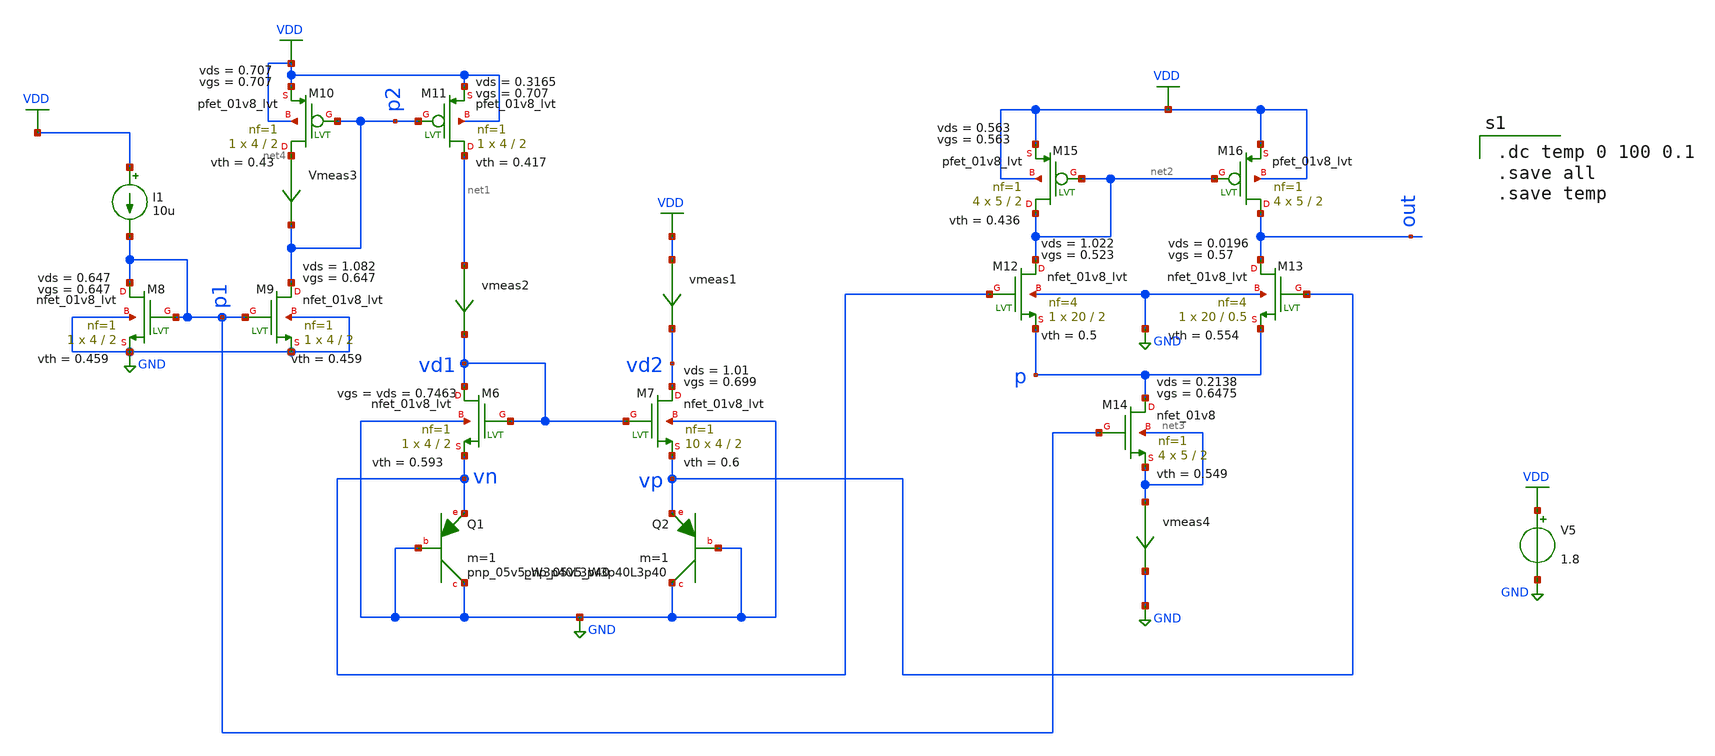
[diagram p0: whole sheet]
** sch_path: ANOTHER_SOLUTIONS_CONSIDERED/ANOTHER_BIAS_FOR_TEMPERATURE_SENSOR/TEMPERATURE_SENSOR/XSCHEM/Temp_Sensor_unbalanced_tb.sch
**.subckt Temp_Sensor_unbalanced_tb
XM6 vd1 vd1 vn GND sky130_fd_pr__nfet_01v8_lvt L=2 W=4 nf=1 ad='int((nf+1)/2) * W/nf * 0.29' as='int((nf+2)/2) * W/nf * 0.29'
+ pd='2*int((nf+1)/2) * (W/nf + 0.29)' ps='2*int((nf+2)/2) * (W/nf + 0.29)' nrd='0.29 / W' nrs='0.29 / W'
+ sa=0 sb=0 sd=0 mult=1 m=1
XQ1 GND GND vn sky130_fd_pr__pnp_05v5_W3p40L3p40 m=1
XM7 vd2 vd1 vp GND sky130_fd_pr__nfet_01v8_lvt L=2 W=4 nf=1 ad='int((nf+1)/2) * W/nf * 0.29' as='int((nf+2)/2) * W/nf * 0.29'
+ pd='2*int((nf+1)/2) * (W/nf + 0.29)' ps='2*int((nf+2)/2) * (W/nf + 0.29)' nrd='0.29 / W' nrs='0.29 / W'
+ sa=0 sb=0 sd=0 mult=10 m=10
XQ2 GND GND vp sky130_fd_pr__pnp_05v5_W3p40L3p40 m=1
V5 VDD GND 1.8
vmeas1 VDD vd2 0
.save i(vmeas1)
vmeas2 net1 vd1 0
.save i(vmeas2)
I1 VDD p1 10u
XM8 p1 p1 GND GND sky130_fd_pr__nfet_01v8_lvt L=2 W=4 nf=1 ad='int((nf+1)/2) * W/nf * 0.29' as='int((nf+2)/2) * W/nf * 0.29'
+ pd='2*int((nf+1)/2) * (W/nf + 0.29)' ps='2*int((nf+2)/2) * (W/nf + 0.29)' nrd='0.29 / W' nrs='0.29 / W'
+ sa=0 sb=0 sd=0 mult=1 m=1
XM9 p2 p1 GND GND sky130_fd_pr__nfet_01v8_lvt L=2 W=4 nf=1 ad='int((nf+1)/2) * W/nf * 0.29' as='int((nf+2)/2) * W/nf * 0.29'
+ pd='2*int((nf+1)/2) * (W/nf + 0.29)' ps='2*int((nf+2)/2) * (W/nf + 0.29)' nrd='0.29 / W' nrs='0.29 / W'
+ sa=0 sb=0 sd=0 mult=1 m=1
XM10 net4 p2 VDD VDD sky130_fd_pr__pfet_01v8_lvt L=2 W=4 nf=1 ad='int((nf+1)/2) * W/nf * 0.29' as='int((nf+2)/2) * W/nf * 0.29'
+ pd='2*int((nf+1)/2) * (W/nf + 0.29)' ps='2*int((nf+2)/2) * (W/nf + 0.29)' nrd='0.29 / W' nrs='0.29 / W'
+ sa=0 sb=0 sd=0 mult=1 m=1
XM11 net1 p2 VDD VDD sky130_fd_pr__pfet_01v8_lvt L=2 W=4 nf=1 ad='int((nf+1)/2) * W/nf * 0.29' as='int((nf+2)/2) * W/nf * 0.29'
+ pd='2*int((nf+1)/2) * (W/nf + 0.29)' ps='2*int((nf+2)/2) * (W/nf + 0.29)' nrd='0.29 / W' nrs='0.29 / W'
+ sa=0 sb=0 sd=0 mult=1 m=1
Vmeas3 net4 p2 0
.save i(vmeas3)
XM12 net2 vn p GND sky130_fd_pr__nfet_01v8_lvt L=2 W=20 nf=4 ad='int((nf+1)/2) * W/nf * 0.29' as='int((nf+2)/2) * W/nf * 0.29'
+ pd='2*int((nf+1)/2) * (W/nf + 0.29)' ps='2*int((nf+2)/2) * (W/nf + 0.29)' nrd='0.29 / W' nrs='0.29 / W'
+ sa=0 sb=0 sd=0 mult=1 m=1
XM13 out vp p GND sky130_fd_pr__nfet_01v8_lvt L=0.5 W=20 nf=4 ad='int((nf+1)/2) * W/nf * 0.29' as='int((nf+2)/2) * W/nf * 0.29'
+ pd='2*int((nf+1)/2) * (W/nf + 0.29)' ps='2*int((nf+2)/2) * (W/nf + 0.29)' nrd='0.29 / W' nrs='0.29 / W'
+ sa=0 sb=0 sd=0 mult=1 m=1
vmeas4 net3 GND 0
.save i(vmeas4)
XM14 p p1 net3 net3 sky130_fd_pr__nfet_01v8 L=2 W=5 nf=1 ad='int((nf+1)/2) * W/nf * 0.29' as='int((nf+2)/2) * W/nf * 0.29'
+ pd='2*int((nf+1)/2) * (W/nf + 0.29)' ps='2*int((nf+2)/2) * (W/nf + 0.29)' nrd='0.29 / W' nrs='0.29 / W'
+ sa=0 sb=0 sd=0 mult=4 m=4
XM15 net2 net2 VDD VDD sky130_fd_pr__pfet_01v8_lvt L=2 W=5 nf=1 ad='int((nf+1)/2) * W/nf * 0.29' as='int((nf+2)/2) * W/nf * 0.29'
+ pd='2*int((nf+1)/2) * (W/nf + 0.29)' ps='2*int((nf+2)/2) * (W/nf + 0.29)' nrd='0.29 / W' nrs='0.29 / W'
+ sa=0 sb=0 sd=0 mult=4 m=4
XM16 out net2 VDD VDD sky130_fd_pr__pfet_01v8_lvt L=2 W=5 nf=1 ad='int((nf+1)/2) * W/nf * 0.29' as='int((nf+2)/2) * W/nf * 0.29'
+ pd='2*int((nf+1)/2) * (W/nf + 0.29)' ps='2*int((nf+2)/2) * (W/nf + 0.29)' nrd='0.29 / W' nrs='0.29 / W'
+ sa=0 sb=0 sd=0 mult=4 m=4
**** begin user architecture code

** opencircuitdesign pdks install
.lib $::SKYWATER_MODELS/sky130.lib.spice tt



.dc temp 0 100 0.1
.save all
.save temp

**** end user architecture code
**.ends
.GLOBAL GND
.GLOBAL VDD
.end
